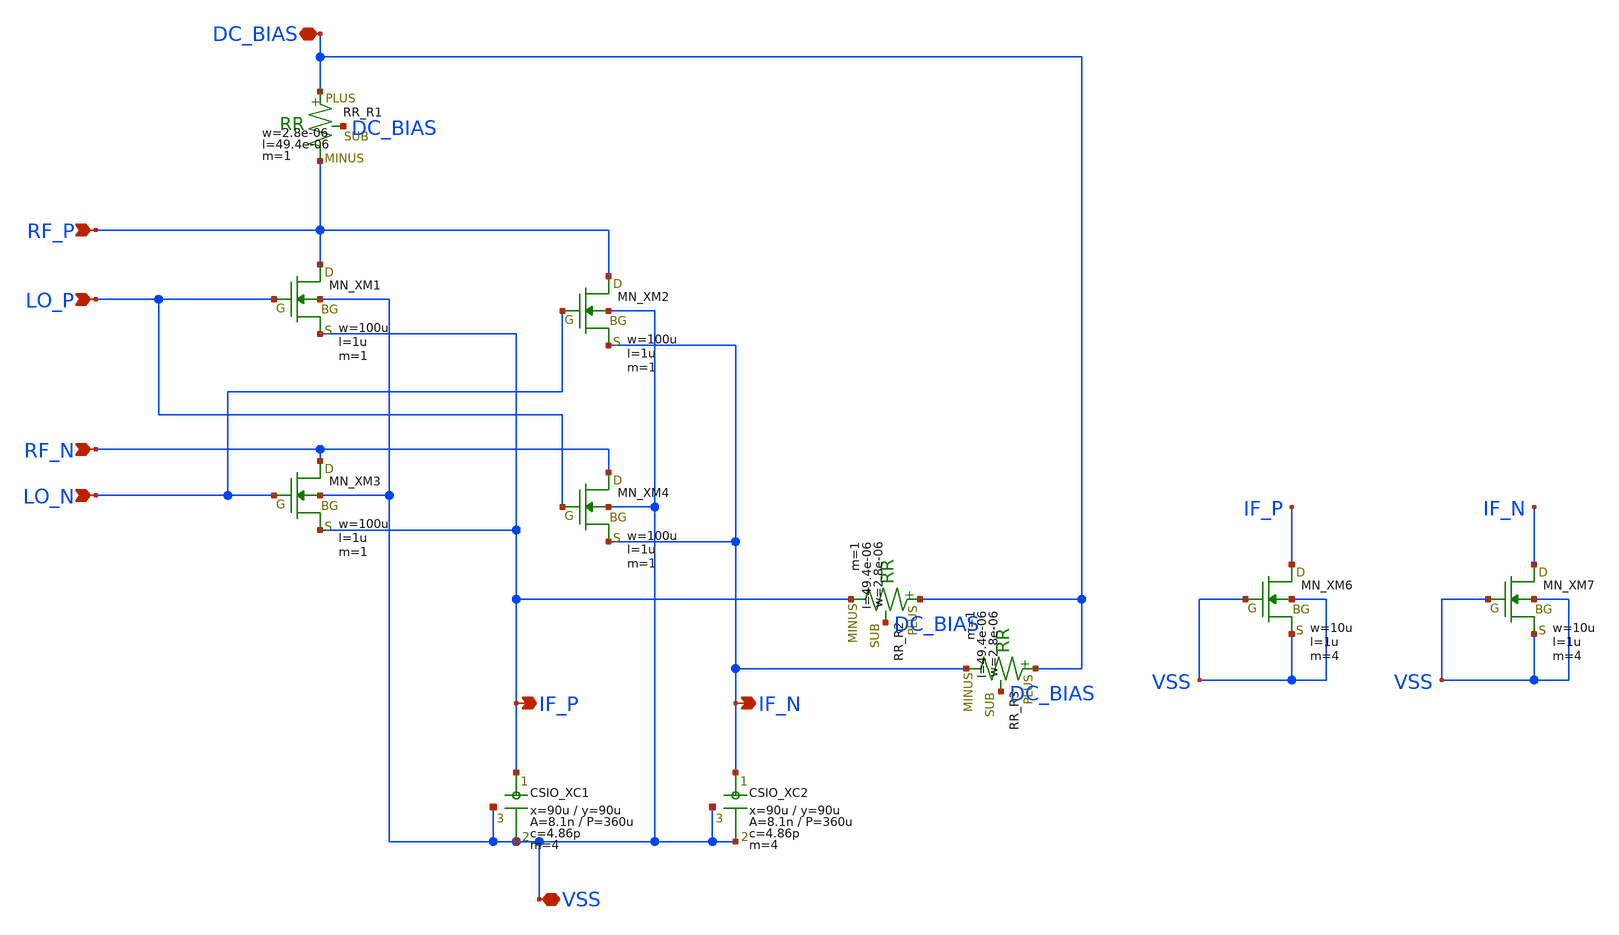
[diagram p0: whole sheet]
** sch_path: member_project/MIXER/noritsuna/xschem/double_balanced_passive_switch_mixer.sch
**.subckt double_balanced_passive_switch_mixer DC_BIAS RF_P LO_P RF_N LO_N IF_N IF_P VSS
*.iopin DC_BIAS
*.ipin RF_P
*.ipin LO_P
*.ipin RF_N
*.ipin LO_N
*.opin IF_N
*.opin IF_P
*.iopin VSS
XXM1 RF_P LO_P IF_P VSS NMOS w=100u l=1u nrd=0 nrs=0 m=1
XXM2 RF_P LO_N IF_N VSS NMOS w=100u l=1u nrd=0 nrs=0 m=1
XXM3 RF_N LO_N IF_P VSS NMOS w=100u l=1u nrd=0 nrs=0 m=1
XXM4 RF_N LO_P IF_N VSS NMOS w=100u l=1u nrd=0 nrs=0 m=1
XR1 DC_BIAS RF_P DC_BIAS F_RR w=2.8e-06 l=49.4e-06 R=20.0e+03 tc1=0 tc2=0 m=1
XR2 DC_BIAS IF_P DC_BIAS F_RR w=2.8e-06 l=49.4e-06 R=20.0e+03 tc1=0 tc2=0 m=1
XXC1 IF_P VSS VSS F_CSIO c=4.86p x=90u y=90u m=4
XXC2 IF_N VSS VSS F_CSIO c=4.86p x=90u y=90u m=4
XR3 DC_BIAS IF_N DC_BIAS F_RR w=2.8e-06 l=49.4e-06 R=20.0e+03 tc1=0 tc2=0 m=1
XXM6 IF_P VSS VSS VSS NMOS w=10u l=1u nrd=0 nrs=0 m=4
XXM7 IF_N VSS VSS VSS NMOS w=10u l=1u nrd=0 nrs=0 m=4
**.ends
.end
